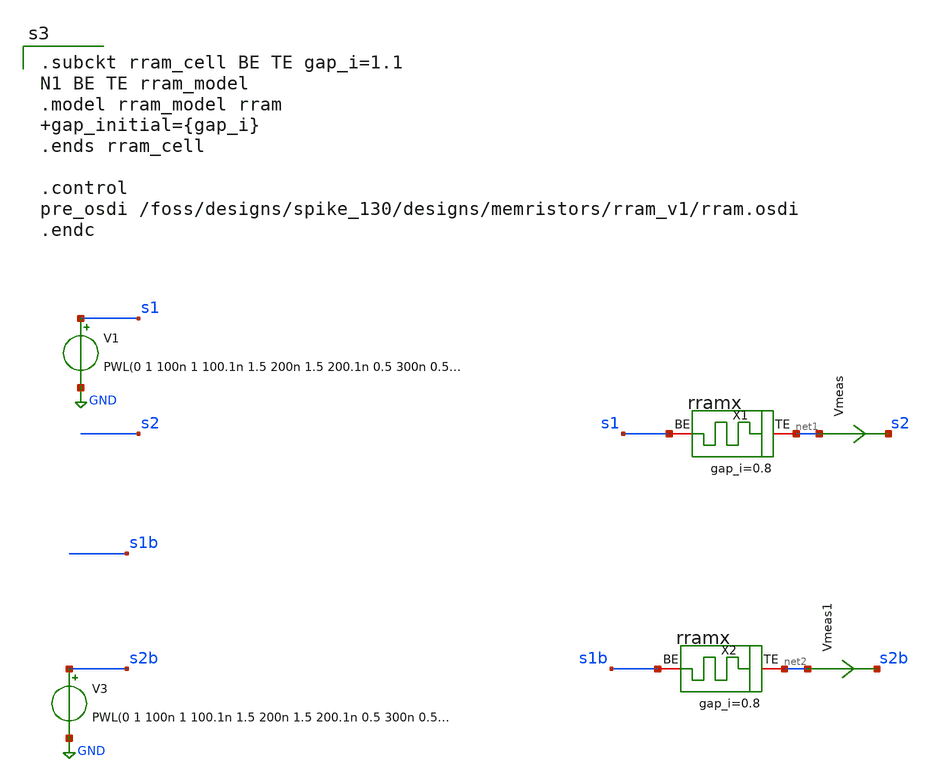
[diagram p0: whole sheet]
** sch_path: designs/tb_memristor/tb_stdp.sch
**.subckt tb_stdp
V1 s1 GND PWL(0 1 100n 1 100.1n 1.5 200n 1.5 200.1n 0.5 300n 0.5 300.1n 1 500n 1 r=0)
Vmeas net1 s2 0
.save i(vmeas)
X1 net1 s1 rram_cell gap_i=0.8
V3 s2b GND PWL(0 1 100n 1 100.1n 1.5 200n 1.5 200.1n 0.5 300n 0.5 300.1n 1 500n 1 r=0)
Vmeas1 net2 s2b 0
.save i(vmeas1)
X2 net2 s1b rram_cell gap_i=0.8
**** begin user architecture code

.subckt rram_cell BE TE gap_i=1.1
N1 BE TE rram_model
.model rram_model rram gap_initial={gap_i}
.ends rram_cell

.control
pre_osdi /foss/designs/spike_130/designs/memristors/rram_v1/rram.osdi
.endc



*------------------ PARAMETROS BASE ------------------
.param t1=110n
.param t2=110.1n
.param t3=210n
.param t4=210.1n
.param t5=300n
.param t6=300.1n

*------------------ FUENTE PWL ------------------
V2 s2 0 PWL( 0 1  {t1} 1  {t2} 1.5  {t3} 1.5  {t4} 0.5  {t5} 0.5  {t6} 1  500n 1 r=0)

V4 s1b 0 PWL( 0 1  {t1} 1  {t2} 1.5  {t3} 1.5  {t4} 0.5  {t5} 0.5  {t6} 1  500n 1 r=0)

.tran 1n 2u

.control
  set wr_singlescale
  set wr_vecnames

  * variables internas del control
  let v1 = 110n
  let v2 = 110.1n
  let v3 = 210n
  let v4 = 210.1n
  let v5 = 300n
  let v6 = 300.1n

  let delta = 10n

  repeat 9

    alterparam t1 = $&v1
    alterparam t2 = $&v2
    alterparam t3 = $&v3
    alterparam t4 = $&v4
    alterparam t5 = $&v5
    alterparam t6 = $&v6

    reset
    run

    *remzerovec
    wrdata tb_stdp.txt v(s1) v(s2) i(vmeas)
		+v(s1b) v(s2b) i(vmeas1)
    write tb_stdp.raw
    set appendwrite

    * incrementar 10ns
    let v1 = v1 + delta
    let v2 = v2 + delta
    let v3 = v3 + delta
    let v4 = v4 + delta
    let v5 = v5 + delta
    let v6 = v6 + delta

  end

.endc
.save all
.end

**** end user architecture code
**.ends
.GLOBAL GND
.end
